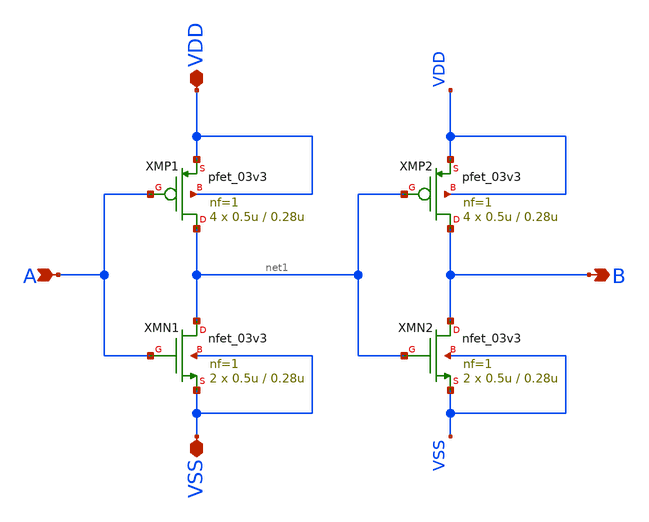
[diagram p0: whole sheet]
** sch_path: designs/sar_adc/digital/gate_buf_x1/xschem/gate_buf_x1.sch
**.subckt gate_buf_x1 B A VDD VSS
*.opin B
*.ipin A
*.iopin VDD
*.iopin VSS
XMN1 net1 A VSS VSS nfet_03v3 L=0.28u W=0.5u nf=1 ad='int((nf+1)/2) * W/nf * 0.18u' as='int((nf+2)/2) * W/nf * 0.18u'
+ pd='2*int((nf+1)/2) * (W/nf + 0.18u)' ps='2*int((nf+2)/2) * (W/nf + 0.18u)' nrd='0.18u / W' nrs='0.18u / W'
+ sa=0 sb=0 sd=0 m=2
XMP1 net1 A VDD VDD pfet_03v3 L=0.28u W=0.5u nf=1 ad='int((nf+1)/2) * W/nf * 0.18u' as='int((nf+2)/2) * W/nf * 0.18u'
+ pd='2*int((nf+1)/2) * (W/nf + 0.18u)' ps='2*int((nf+2)/2) * (W/nf + 0.18u)' nrd='0.18u / W' nrs='0.18u / W'
+ sa=0 sb=0 sd=0 m=4
XMN2 B net1 VSS VSS nfet_03v3 L=0.28u W=0.5u nf=1 ad='int((nf+1)/2) * W/nf * 0.18u' as='int((nf+2)/2) * W/nf * 0.18u'
+ pd='2*int((nf+1)/2) * (W/nf + 0.18u)' ps='2*int((nf+2)/2) * (W/nf + 0.18u)' nrd='0.18u / W' nrs='0.18u / W'
+ sa=0 sb=0 sd=0 m=2
XMP2 B net1 VDD VDD pfet_03v3 L=0.28u W=0.5u nf=1 ad='int((nf+1)/2) * W/nf * 0.18u' as='int((nf+2)/2) * W/nf * 0.18u'
+ pd='2*int((nf+1)/2) * (W/nf + 0.18u)' ps='2*int((nf+2)/2) * (W/nf + 0.18u)' nrd='0.18u / W' nrs='0.18u / W'
+ sa=0 sb=0 sd=0 m=4
**.ends
.end
